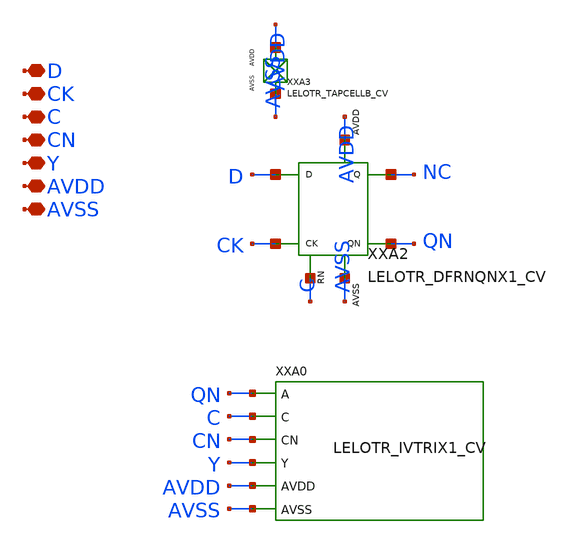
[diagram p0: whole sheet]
** sch_path: design/LELO_TR_GF180MCUD/LELOTR_DFTRIX1_CV.sch
**.subckt LELOTR_DFTRIX1_CV D CK C CN Y AVDD AVSS
*.iopin D
*.iopin CK
*.iopin C
*.iopin CN
*.iopin Y
*.iopin AVDD
*.iopin AVSS
XXA3 AVDD AVSS LELOTR_TAPCELLB_CV xoffset=0 yoffset=0 angle=0
XXA2 D CK C NC QN AVDD AVSS LELOTR_DFRNQNX1_CV
XXA0 QN C CN Y AVDD AVSS LELOTR_IVTRIX1_CV
**.ends
.end
